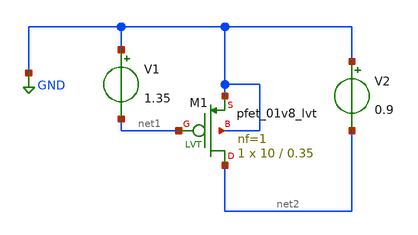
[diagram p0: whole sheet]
** sch_path: MOS-Design-Parameters/PMOS/act6_ro.sch
**.subckt act6_ro
XM1 net2 net1 GND GND sky130_fd_pr__pfet_01v8_lvt L=0.35 W=10 nf=1 ad='int((nf+1)/2) * W/nf * 0.29' as='int((nf+2)/2) * W/nf * 0.29'
+ pd='2*int((nf+1)/2) * (W/nf + 0.29)' ps='2*int((nf+2)/2) * (W/nf + 0.29)' nrd='0.29 / W' nrs='0.29 / W'
+ sa=0 sb=0 sd=0 mult=1 m=1
V1 GND net1 1.35
V2 GND net2 0.9
**** begin user architecture code



.lib /usr/local/share/pdk/sky130A/libs.tech/ngspice/sky130.lib.spice ff
.option wnflag=1 scale=1e-6

.control

save all
save @m.xm1.msky130_fd_pr__pfet_01v8_lvt[gds]

dc v2 0 1.8 1m

let gds = @m.xm1.msky130_fd_pr__pfet_01v8_lvt[gds]
let ro = 1/gds

wrdata ro-ff.txt ro

.endc


**** end user architecture code
**.ends
.GLOBAL GND
.end
